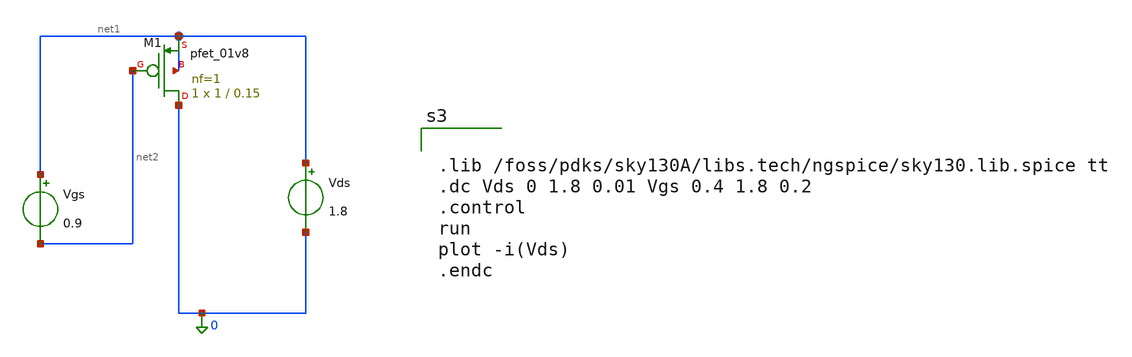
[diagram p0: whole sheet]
** sch_path: week1_mos_characterization/pmos_iv.sch
**.subckt pmos_iv
Vgs net1 net2 0.9
Vds net1 0 1.8
XM1 0 net2 net1 net1 sky130_fd_pr__pfet_01v8 L=0.15 W=1 nf=1 ad='int((1 + 1)/2) * 1 / 1 * 0.29' as='int((1 + 2)/2) * 1 / 1 * 0.29'
+ pd='2*int((1 + 1)/2) * (1 / 1 + 0.29)' ps='2*int((1 + 2)/2) * (1 / 1 + 0.29)' nrd='0.29 / 1 ' nrs='0.29 / 1 '
+ sa=0 sb=0 sd=0 mult=1 m=1
**** begin user architecture code


.lib /foss/pdks/sky130A/libs.tech/ngspice/sky130.lib.spice tt
.dc Vds 0 1.8 0.01 Vgs 0.4 1.8 0.2
.control
run
plot -i(Vds)
.endc


**** end user architecture code
**.ends
.end
